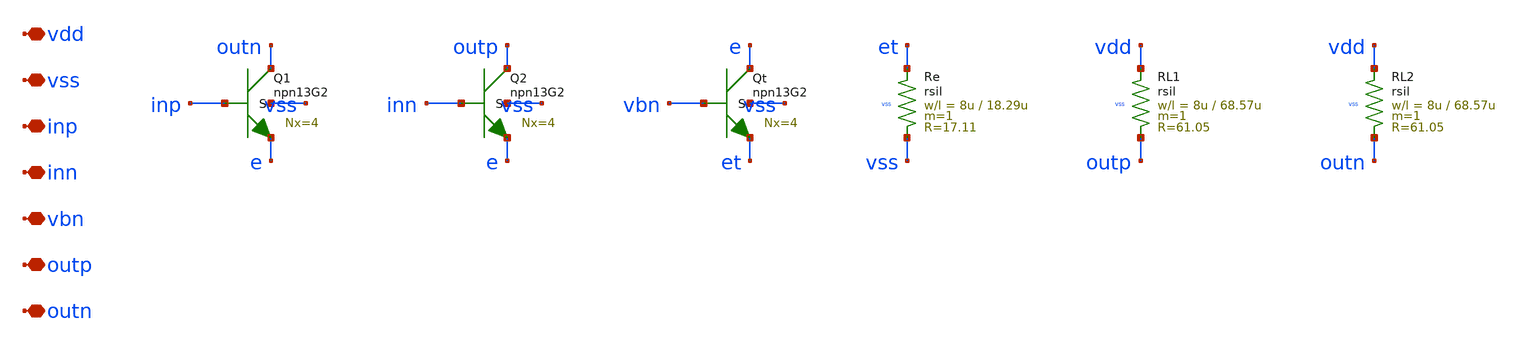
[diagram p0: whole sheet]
** sch_path: design/tx/predriver.sch
**.subckt predriver vdd vss inp inn vbn outp outn
*.iopin vdd
*.iopin vss
*.iopin inp
*.iopin inn
*.iopin vbn
*.iopin outp
*.iopin outn
XQ1 outn inp e vss npn13G2 Nx=4 mm_ok=1
XQ2 outp inn e vss npn13G2 Nx=4 mm_ok=1
XQt e vbn et vss npn13G2 Nx=4 mm_ok=1
XRe et vss vss rsil w=8u l=18.29u m=1 mm_ok=1
XRL1 vdd outp vss rsil w=8u l=68.57u m=1 mm_ok=1
XRL2 vdd outn vss rsil w=8u l=68.57u m=1 mm_ok=1
**.ends
.end
